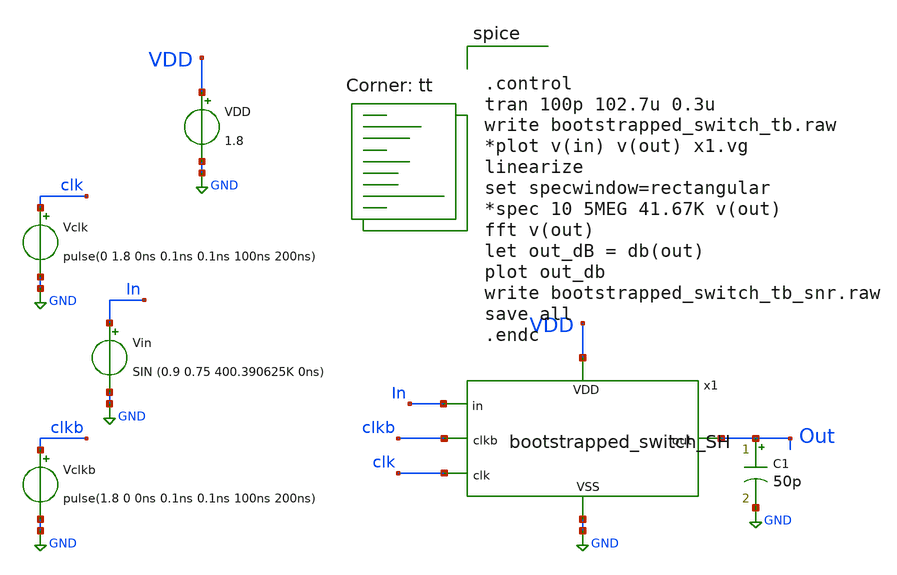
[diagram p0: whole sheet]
** sch_path: bootstrapped_switch_tb.sch
**.subckt bootstrapped_switch_tb
Vclk clk GND pulse(0 1.8 0ns 0.1ns 0.1ns 100ns 200ns)
Vin In GND SIN (0.9 0.75 400.390625K 0ns)
VDD VDD GND 1.8
Vclkb clkb GND pulse(1.8 0 0ns 0.1ns 0.1ns 100ns 200ns)
x1 VDD In clkb clk Out GND bootstrapped_switch_SH
C1 Out GND 50p m=1
**** begin user architecture code
.lib $::SKYWATER_MODELS/sky130.lib.spice tt


.control
tran 100p 102.7u 0.3u
write bootstrapped_switch_tb.raw
*plot v(in) v(out) x1.vg
linearize
set specwindow=rectangular
*spec 10 5MEG 41.67K v(out)
fft v(out)
let out_dB = db(out)
plot out_db
write bootstrapped_switch_tb_snr.raw
save all
.endc


**** end user architecture code
**.ends

* expanding   symbol:  bootstrapped_switch_SH.sym # of pins=6
** sym_path: bootstrapped_switch_SH.sym
** sch_path: bootstrapped_switch_SH.sch
.subckt bootstrapped_switch_SH VDD in clkb clk out VSS
*.ipin in
*.opin out
*.ipin VSS
*.ipin VDD
*.ipin clkb
*.ipin clk
XM1 net3 clkb net4 net4 sky130_fd_pr__nfet_01v8 L=0.15 W=2 nf=1 ad='int((nf+1)/2) * W/nf * 0.29' as='int((nf+2)/2) * W/nf * 0.29'
+ pd='2*int((nf+1)/2) * (W/nf + 0.29)' ps='2*int((nf+2)/2) * (W/nf + 0.29)' nrd='0.29 / W' nrs='0.29 / W'
+ sa=0 sb=0 sd=0 mult=1 m=1
XM2 in Vg net3 VSS sky130_fd_pr__nfet_01v8 L=1 W=0.5 nf=1 ad='int((nf+1)/2) * W/nf * 0.29' as='int((nf+2)/2) * W/nf * 0.29'
+ pd='2*int((nf+1)/2) * (W/nf + 0.29)' ps='2*int((nf+2)/2) * (W/nf + 0.29)' nrd='0.29 / W' nrs='0.29 / W'
+ sa=0 sb=0 sd=0 mult=1 m=1
XM3 Vp Vg net1 Vp sky130_fd_pr__pfet_01v8 L=0.15 W=2 nf=1 ad='int((nf+1)/2) * W/nf * 0.29' as='int((nf+2)/2) * W/nf * 0.29'
+ pd='2*int((nf+1)/2) * (W/nf + 0.29)' ps='2*int((nf+2)/2) * (W/nf + 0.29)' nrd='0.29 / W' nrs='0.29 / W'
+ sa=0 sb=0 sd=0 mult=1 m=1
XM5 out Vg in VSS sky130_fd_pr__nfet_01v8 L=0.15 W=30 nf=1 ad='int((nf+1)/2) * W/nf * 0.29' as='int((nf+2)/2) * W/nf * 0.29'
+ pd='2*int((nf+1)/2) * (W/nf + 0.29)' ps='2*int((nf+2)/2) * (W/nf + 0.29)' nrd='0.29 / W' nrs='0.29 / W'
+ sa=0 sb=0 sd=0 mult=1 m=1
XM6 out clkb in VDD sky130_fd_pr__pfet_01v8 L=0.15 W=30 nf=1 ad='int((nf+1)/2) * W/nf * 0.29' as='int((nf+2)/2) * W/nf * 0.29'
+ pd='2*int((nf+1)/2) * (W/nf + 0.29)' ps='2*int((nf+2)/2) * (W/nf + 0.29)' nrd='0.29 / W' nrs='0.29 / W'
+ sa=0 sb=0 sd=0 mult=1 m=1
XM8 net5 clkb net2 net2 sky130_fd_pr__nfet_01v8 L=0.15 W=0.5 nf=1 ad='int((nf+1)/2) * W/nf * 0.29' as='int((nf+2)/2) * W/nf * 0.29'
+ pd='2*int((nf+1)/2) * (W/nf + 0.29)' ps='2*int((nf+2)/2) * (W/nf + 0.29)' nrd='0.29 / W' nrs='0.29 / W'
+ sa=0 sb=0 sd=0 mult=1 m=1
XCb net3 Vp sky130_fd_pr__cap_mim_m3_1 W=18 L=18 MF=10 m=10
XM7 Vg VDD net5 net5 sky130_fd_pr__nfet_01v8 L=0.15 W=0.5 nf=1 ad='int((nf+1)/2) * W/nf * 0.29' as='int((nf+2)/2) * W/nf * 0.29'
+ pd='2*int((nf+1)/2) * (W/nf + 0.29)' ps='2*int((nf+2)/2) * (W/nf + 0.29)' nrd='0.29 / W' nrs='0.29 / W'
+ sa=0 sb=0 sd=0 mult=1 m=1
XM4 Vg clkb Vp Vp sky130_fd_pr__pfet_01v8 L=0.15 W=0.5 nf=1 ad='int((nf+1)/2) * W/nf * 0.29' as='int((nf+2)/2) * W/nf * 0.29'
+ pd='2*int((nf+1)/2) * (W/nf + 0.29)' ps='2*int((nf+2)/2) * (W/nf + 0.29)' nrd='0.29 / W' nrs='0.29 / W'
+ sa=0 sb=0 sd=0 mult=1 m=1
XM10 net1 clk net6 net1 sky130_fd_pr__pfet_01v8 L=0.15 W=2 nf=1 ad='int((nf+1)/2) * W/nf * 0.29' as='int((nf+2)/2) * W/nf * 0.29'
+ pd='2*int((nf+1)/2) * (W/nf + 0.29)' ps='2*int((nf+2)/2) * (W/nf + 0.29)' nrd='0.29 / W' nrs='0.29 / W'
+ sa=0 sb=0 sd=0 mult=1 m=1
XM11 net4 clkb net7 net7 sky130_fd_pr__nfet_01v8 L=0.15 W=2 nf=1 ad='int((nf+1)/2) * W/nf * 0.29' as='int((nf+2)/2) * W/nf * 0.29'
+ pd='2*int((nf+1)/2) * (W/nf + 0.29)' ps='2*int((nf+2)/2) * (W/nf + 0.29)' nrd='0.29 / W' nrs='0.29 / W'
+ sa=0 sb=0 sd=0 mult=1 m=1
XM12 net6 clk VDD net6 sky130_fd_pr__pfet_01v8 L=0.15 W=2 nf=1 ad='int((nf+1)/2) * W/nf * 0.29' as='int((nf+2)/2) * W/nf * 0.29'
+ pd='2*int((nf+1)/2) * (W/nf + 0.29)' ps='2*int((nf+2)/2) * (W/nf + 0.29)' nrd='0.29 / W' nrs='0.29 / W'
+ sa=0 sb=0 sd=0 mult=1 m=1
XM13 net7 clkb VSS VSS sky130_fd_pr__nfet_01v8 L=0.15 W=2 nf=1 ad='int((nf+1)/2) * W/nf * 0.29' as='int((nf+2)/2) * W/nf * 0.29'
+ pd='2*int((nf+1)/2) * (W/nf + 0.29)' ps='2*int((nf+2)/2) * (W/nf + 0.29)' nrd='0.29 / W' nrs='0.29 / W'
+ sa=0 sb=0 sd=0 mult=1 m=1
XM14 net2 clkb VSS VSS sky130_fd_pr__nfet_01v8 L=0.15 W=0.5 nf=1 ad='int((nf+1)/2) * W/nf * 0.29' as='int((nf+2)/2) * W/nf * 0.29'
+ pd='2*int((nf+1)/2) * (W/nf + 0.29)' ps='2*int((nf+2)/2) * (W/nf + 0.29)' nrd='0.29 / W' nrs='0.29 / W'
+ sa=0 sb=0 sd=0 mult=1 m=1
XC2 out VSS sky130_fd_pr__cap_mim_m3_1 W=36 L=36 MF=20 m=20
.ends

.GLOBAL GND
.end
